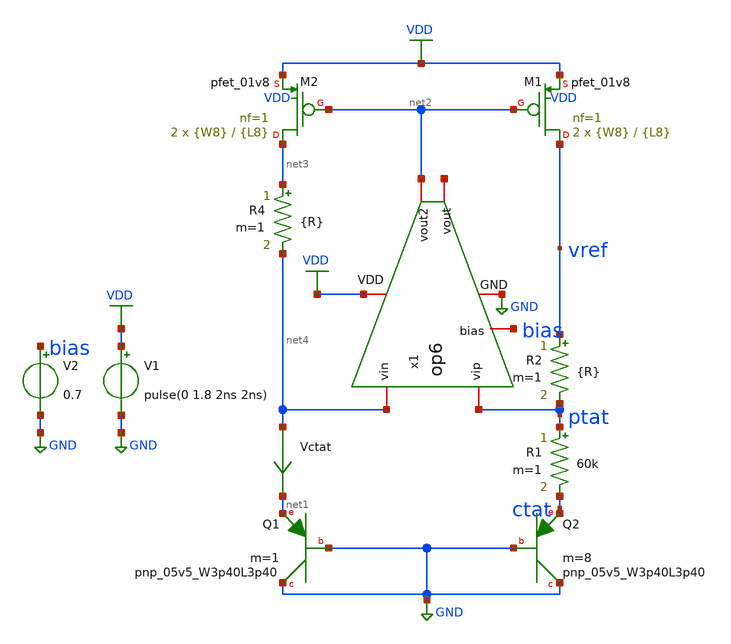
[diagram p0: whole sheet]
** sch_path: xschem/bgr_op7.sch
**.subckt bgr_op7
XQ1 GND GND net1 sky130_fd_pr__pnp_05v5_W3p40L3p40 m=1
XQ2 GND GND ctat sky130_fd_pr__pnp_05v5_W3p40L3p40 m=8
Vctat net4 net1 0
.save i(vctat)
V1 VDD GND pulse(0 1.8 2ns 2ns)
XM1 vref net2 VDD VDD sky130_fd_pr__pfet_01v8 L={L8} W={W8} nf=1 ad='int((nf+1)/2) * W/nf * 0.29' as='int((nf+2)/2) * W/nf * 0.29'
+ pd='2*int((nf+1)/2) * (W/nf + 0.29)' ps='2*int((nf+2)/2) * (W/nf + 0.29)' nrd='0.29 / W' nrs='0.29 / W'
+ sa=0 sb=0 sd=0 mult=2 m=2
XM2 net3 net2 VDD VDD sky130_fd_pr__pfet_01v8 L={L8} W={W8} nf=1 ad='int((nf+1)/2) * W/nf * 0.29' as='int((nf+2)/2) * W/nf * 0.29'
+ pd='2*int((nf+1)/2) * (W/nf + 0.29)' ps='2*int((nf+2)/2) * (W/nf + 0.29)' nrd='0.29 / W' nrs='0.29 / W'
+ sa=0 sb=0 sd=0 mult=2 m=2
R1 ptat ctat 60k m=1
R2 vref ptat {R} m=1
R4 net3 net4 {R} m=1
x1 VDD net4 ptat net2 net5 bias GND op6
V2 bias GND 0.7
**** begin user architecture code


.param L8=1
.param W8=1
.param R=608k



** opencircuitdesign pdks install
.lib $::SKYWATER_MODELS/sky130.lib.spice tt




.option savecurrents
.control
save all
op
remzerovec
write bgr_op7.raw
set appendwrite

dc temp -40 85 1
remzerovec
write bgr_op7.raw
*plot (ptat-ctat)
*plot ctat
plot vref

********TC********
meas dc temp_avg_vref avg v(vref)
meas dc temp_vref_27 find v(vref) when temp-sweep=27
meas dc temp_pp_vref PP v(vref)
meas dc temp_vref_max max v(vref)
meas dc temp_max_vref when v(vref)='temp_vref_max'
meas dc temp_vref_min min v(vref)
meas dc temp_min_vref when v(vref)='temp_vref_min'
let vref_tc='((temp_pp_vref*1000000)/(125*temp_avg_vref))'
print vref_tc

******PSRR******
ac dec 1000 1 10Meg
write bgr_op7.raw
remzerovec
plot vdb(vref)
meas ac psrr_100 find vdb(vref) at=100
meas ac psrr_1k find vdb(vref) at=1k

****Power****
tran 1 2
write bgr_op7.raw
remzerovec
meas tran ave_v avg vdd
meas tran ave_i avg i(v1)
let ave_power='ave_v*(-ave_i)
plot vdd vref
*plot -i(v1)
print ave_power

*******LS******
dc v1 0 3.5 0.1
write bgr_op7.raw
remzerovec
meas dc vref_max max v(vref) from=1.62 to=1.98
meas dc vref_min min v(vref) from=1.62 to=1.98
let line_reg='100*(vref_max-vref_min)/vref_min/(1.98-1.62)'
print line_reg
plot vdd vref

.endc


**** end user architecture code
**.ends

* expanding   symbol:  op6.sym # of pins=7
** sym_path: xschem/op6.sym
** sch_path: xschem/op6.sch
.subckt op6 VDD vin vip vout2 vout bias GND
*.iopin VDD
*.iopin GND
*.iopin vout
*.iopin vip
*.iopin vin
*.iopin vout2
*.iopin bias
XM1 net1 net1 VDD VDD sky130_fd_pr__pfet_01v8 L={L1} W={W1} nf=1 ad='int((nf+1)/2) * W/nf * 0.29' as='int((nf+2)/2)
+ * W/nf * 0.29' pd='2*int((nf+1)/2) * (W/nf + 0.29)' ps='2*int((nf+2)/2) * (W/nf + 0.29)' nrd='0.29 /
+ W' nrs='0.29 / W' sa=0 sb=0 sd=0 mult={M1} m={M1}
XM2 net2 net2 net1 VDD sky130_fd_pr__pfet_01v8 L={L1} W={W1} nf=1 ad='int((nf+1)/2) * W/nf * 0.29' as='int((nf+2)/2)
+ * W/nf * 0.29' pd='2*int((nf+1)/2) * (W/nf + 0.29)' ps='2*int((nf+2)/2) * (W/nf + 0.29)' nrd='0.29 /
+ W' nrs='0.29 / W' sa=0 sb=0 sd=0 mult={M1} m={M1}
XM3 net4 net1 VDD VDD sky130_fd_pr__pfet_01v8 L={L6} W={W6} nf=1 ad='int((nf+1)/2) * W/nf * 0.29' as='int((nf+2)/2)
+ * W/nf * 0.29' pd='2*int((nf+1)/2) * (W/nf + 0.29)' ps='2*int((nf+2)/2) * (W/nf + 0.29)' nrd='0.29 /
+ W' nrs='0.29 / W' sa=0 sb=0 sd=0 mult={M6} m={M6}
XM4 net3 net2 net4 VDD sky130_fd_pr__pfet_01v8 L={L6} W={W6} nf=1 ad='int((nf+1)/2) * W/nf * 0.29' as='int((nf+2)/2)
+ * W/nf * 0.29' pd='2*int((nf+1)/2) * (W/nf + 0.29)' ps='2*int((nf+2)/2) * (W/nf + 0.29)' nrd='0.29 /
+ W' nrs='0.29 / W' sa=0 sb=0 sd=0 mult={M6} m={M6}
XM5 net5 net1 VDD VDD sky130_fd_pr__pfet_01v8 L={L5} W={W5} nf=1 ad='int((nf+1)/2) * W/nf * 0.29' as='int((nf+2)/2)
+ * W/nf * 0.29' pd='2*int((nf+1)/2) * (W/nf + 0.29)' ps='2*int((nf+2)/2) * (W/nf + 0.29)' nrd='0.29 /
+ W' nrs='0.29 / W' sa=0 sb=0 sd=0 mult={M5} m={M5}
XM6 vout2 net2 net5 VDD sky130_fd_pr__pfet_01v8 L={L5} W={W5} nf=1 ad='int((nf+1)/2) * W/nf * 0.29' as='int((nf+2)/2)
+ * W/nf * 0.29' pd='2*int((nf+1)/2) * (W/nf + 0.29)' ps='2*int((nf+2)/2) * (W/nf + 0.29)' nrd='0.29 /
+ W' nrs='0.29 / W' sa=0 sb=0 sd=0 mult={M5} m={M5}
XM7 net6 vin net3 VDD sky130_fd_pr__pfet_01v8 L={L2} W={W2} nf=1 ad='int((nf+1)/2) * W/nf * 0.29' as='int((nf+2)/2)
+ * W/nf * 0.29' pd='2*int((nf+1)/2) * (W/nf + 0.29)' ps='2*int((nf+2)/2) * (W/nf + 0.29)' nrd='0.29 /
+ W' nrs='0.29 / W' sa=0 sb=0 sd=0 mult={M2} m={M2}
XM8 vout vip net3 VDD sky130_fd_pr__pfet_01v8 L={L2} W={W2} nf=1 ad='int((nf+1)/2) * W/nf * 0.29' as='int((nf+2)/2)
+ * W/nf * 0.29' pd='2*int((nf+1)/2) * (W/nf + 0.29)' ps='2*int((nf+2)/2) * (W/nf + 0.29)' nrd='0.29 /
+ W' nrs='0.29 / W' sa=0 sb=0 sd=0 mult={M2} m={M2}
XM9 vout net6 GND GND sky130_fd_pr__nfet_01v8 L={L3} W={W3} nf=1 ad='int((nf+1)/2) * W/nf * 0.29' as='int((nf+2)/2)
+ * W/nf * 0.29' pd='2*int((nf+1)/2) * (W/nf + 0.29)' ps='2*int((nf+2)/2) * (W/nf + 0.29)' nrd='0.29 /
+ W' nrs='0.29 / W' sa=0 sb=0 sd=0 mult={M3} m={M3}
XM10 net6 net6 GND GND sky130_fd_pr__nfet_01v8 L={L3} W={W3} nf=1 ad='int((nf+1)/2) * W/nf * 0.29' as='int((nf+2)/2)
+ * W/nf * 0.29' pd='2*int((nf+1)/2) * (W/nf + 0.29)' ps='2*int((nf+2)/2) * (W/nf + 0.29)' nrd='0.29 /
+ W' nrs='0.29 / W' sa=0 sb=0 sd=0 mult={M3} m={M3}
XM11 vout2 vout GND GND sky130_fd_pr__nfet_01v8 L={L4} W={W4} nf=1 ad='int((nf+1)/2) * W/nf * 0.29' as='int((nf+2)/2)
+ * W/nf * 0.29' pd='2*int((nf+1)/2) * (W/nf + 0.29)' ps='2*int((nf+2)/2) * (W/nf + 0.29)' nrd='0.29 /
+ W' nrs='0.29 / W' sa=0 sb=0 sd=0 mult={M4} m={M4}
XM12 net2 bias GND GND sky130_fd_pr__nfet_01v8 L={L7} W={W7} nf=1 ad='int((nf+1)/2) * W/nf * 0.29' as='int((nf+2)/2)
+ * W/nf * 0.29' pd='2*int((nf+1)/2) * (W/nf + 0.29)' ps='2*int((nf+2)/2) * (W/nf + 0.29)' nrd='0.29 /
+ W' nrs='0.29 / W' sa=0 sb=0 sd=0 mult={M7} m={M7}
C1 vout2 net7 1p m=1
R1 net7 vout 1k m=1
**** begin user architecture code


***PMOS***
.param L1=1
.param W1=1
.param M1=4

***NMOS current source***
.param L7=1
.param W7=10
.param M7=4

***Diffpair***
.param L2=2.5
.param W2=35
.param M2=4

***NMOS load***
.param L3=2
.param W3=15
.param M3=4

***NMOS second stage***
.param L4=5
.param W4=30
.param M4=4

***PMOS current source second***
.param L5=0.4
.param W5=7
.param M5=4

***PMOS current source***
.param L6=0.4
.param W6=7
.param M6=4


**** end user architecture code
.ends

.GLOBAL VDD
.GLOBAL GND
.end
